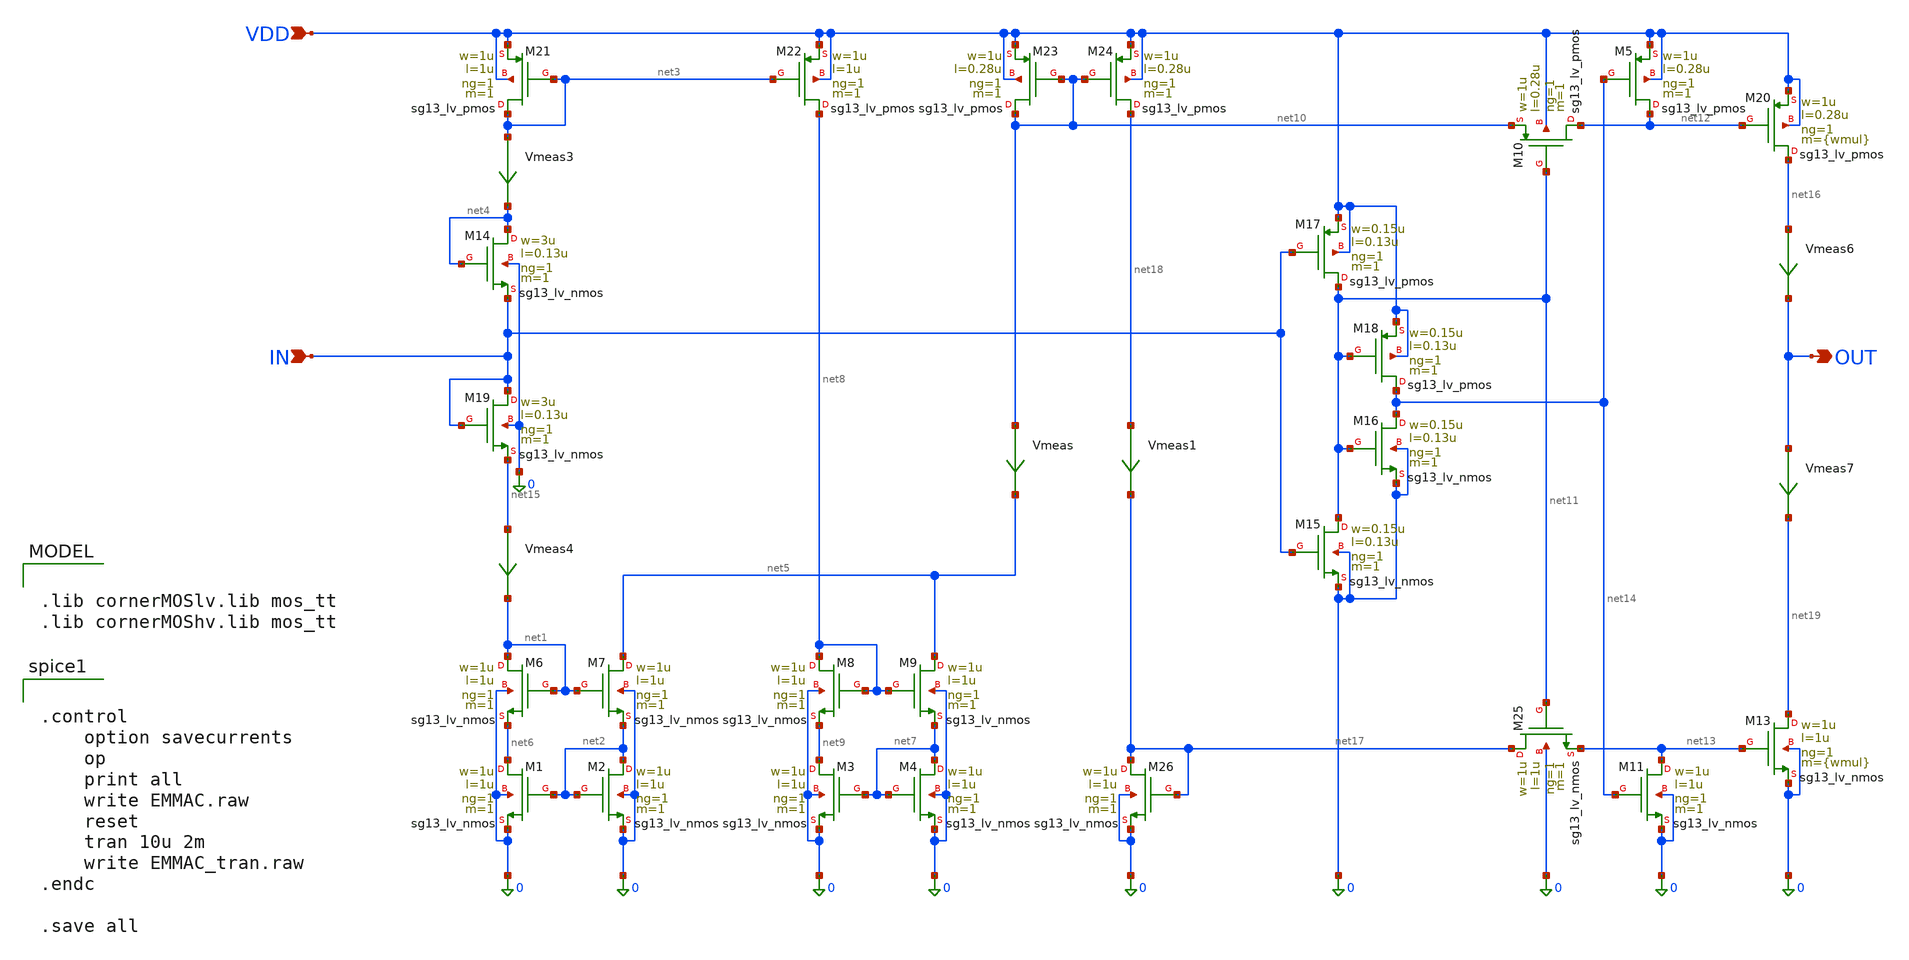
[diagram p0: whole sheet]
** sch_path: src/analog_mac/EMMAC_Block_v3.sch
**.subckt EMMAC_Block_v3 OUT IN VDD
*.opin OUT
*.ipin IN
*.ipin VDD
XM1 net6 net2 0 0 sg13_lv_nmos w=1u l=1u ng=1 m=1 mm_ok=1
XM2 net2 net2 0 0 sg13_lv_nmos w=1u l=1u ng=1 m=1 mm_ok=1
XM21 net3 net3 VDD VDD sg13_lv_pmos w=1u l=1u ng=1 m=1 mm_ok=1
XM22 net8 net3 VDD VDD sg13_lv_pmos w=1u l=1u ng=1 m=1 mm_ok=1
XM6 net1 net1 net6 0 sg13_lv_nmos w=1u l=1u ng=1 m=1 mm_ok=1
XM7 net5 net1 net2 0 sg13_lv_nmos w=1u l=1u ng=1 m=1 mm_ok=1
XM3 net9 net7 0 0 sg13_lv_nmos w=1u l=1u ng=1 m=1 mm_ok=1
XM4 net7 net7 0 0 sg13_lv_nmos w=1u l=1u ng=1 m=1 mm_ok=1
XM8 net8 net8 net9 0 sg13_lv_nmos w=1u l=1u ng=1 m=1 mm_ok=1
XM9 net5 net8 net7 0 sg13_lv_nmos w=1u l=1u ng=1 m=1 mm_ok=1
XM23 net10 net10 VDD VDD sg13_lv_pmos w=1u l=0.28u ng=1 m=1 mm_ok=1
XM24 net18 net10 VDD VDD sg13_lv_pmos w=1u l=0.28u ng=1 m=1 mm_ok=1
XM20 net16 net12 VDD VDD sg13_lv_pmos w=1u l=0.28u ng=1 m={wmul} mm_ok=1
XM13 net19 net13 0 0 sg13_lv_nmos w=1u l=1u ng=1 m={wmul} mm_ok=1
XM15 net11 IN 0 0 sg13_lv_nmos w=0.15u l=0.13u ng=1 m=1 mm_ok=1
XM17 net11 IN VDD VDD sg13_lv_pmos w=0.15u l=0.13u ng=1 m=1 mm_ok=1
XM16 net14 net11 0 0 sg13_lv_nmos w=0.15u l=0.13u ng=1 m=1 mm_ok=1
XM18 net14 net11 VDD VDD sg13_lv_pmos w=0.15u l=0.13u ng=1 m=1 mm_ok=1
XM26 net17 net17 0 0 sg13_lv_nmos w=1u l=1u ng=1 m=1 mm_ok=1
XM5 net12 net14 VDD VDD sg13_lv_pmos w=1u l=0.28u ng=1 m=1 mm_ok=1
XM10 net12 net11 net10 VDD sg13_lv_pmos w=1u l=0.28u ng=1 m=1 mm_ok=1
XM11 net13 net14 0 0 sg13_lv_nmos w=1u l=1u ng=1 m=1 mm_ok=1
XM25 net17 net11 net13 0 sg13_lv_nmos w=1u l=1u ng=1 m=1 mm_ok=1
Vmeas net10 net5 0
.save i(vmeas)
Vmeas1 net18 net17 0
.save i(vmeas1)
Vmeas3 net3 net4 0
.save i(vmeas3)
Vmeas4 net15 net1 0
.save i(vmeas4)
Vmeas6 net16 OUT 0
.save i(vmeas6)
Vmeas7 OUT net19 0
.save i(vmeas7)
XM14 net4 net4 IN 0 sg13_lv_nmos w=3u l=0.13u ng=1 m=1 mm_ok=1
XM19 IN IN net15 0 sg13_lv_nmos w=3u l=0.13u ng=1 m=1 mm_ok=1
**** begin user architecture code

.lib cornerMOSlv.lib mos_tt
.lib cornerMOShv.lib mos_tt



.control
	option savecurrents
	op
	print all
	write EMMAC.raw
	reset
	tran 10u 2m
	write EMMAC_tran.raw
.endc

.save all


**** end user architecture code
**.ends
.end
